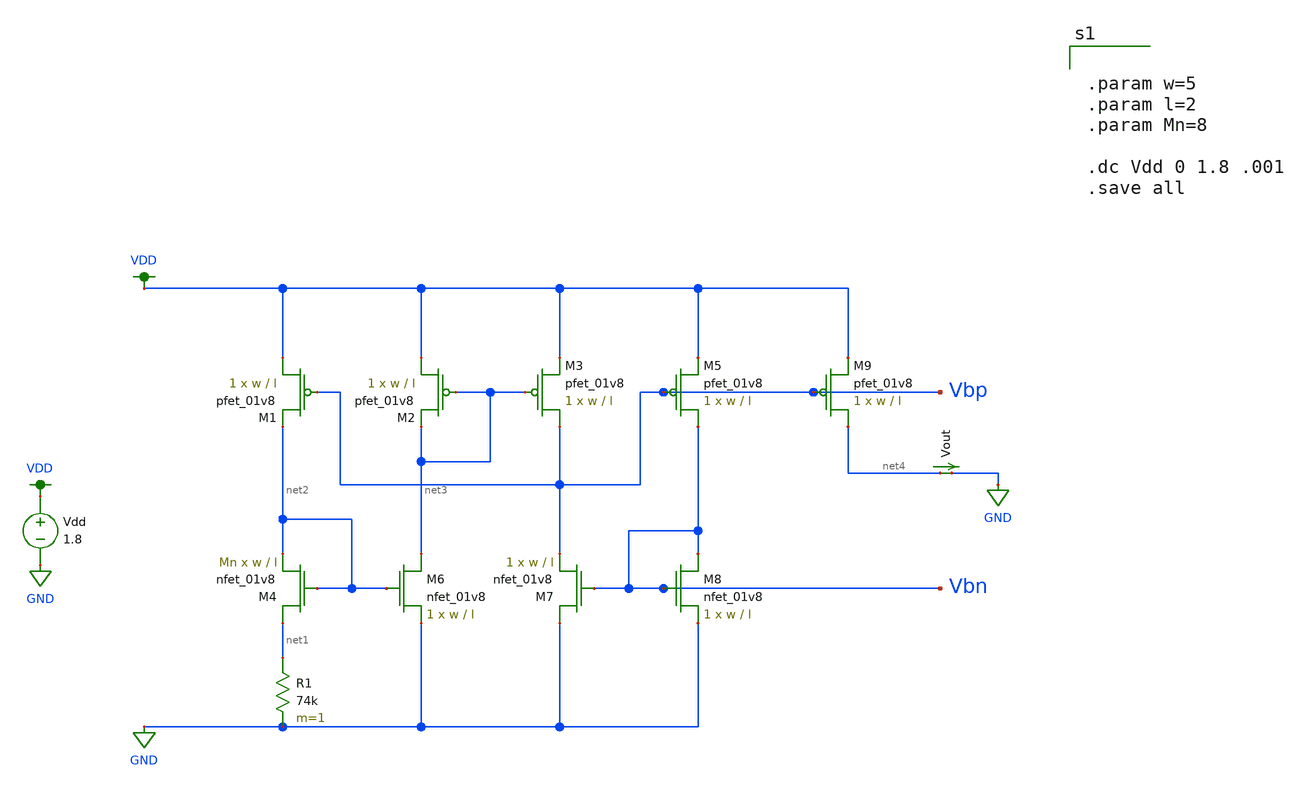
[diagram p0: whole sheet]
** sch_path: schematic/test/bias_current_resistive.sch
**.subckt bias_current_resistive
XM1 VDD Vbp net2 VDD sky130_fd_pr__pfet_01v8 L=l W=w nf=1 ad='int((nf+1)/2) * W/nf * 0.29' as='int((nf+2)/2) * W/nf * 0.29'
+ pd='2*int((nf+1)/2) * (W/nf + 0.29)' ps='2*int((nf+2)/2) * (W/nf + 0.29)' nrd='0.29 / W' nrs='0.29 / W'
+ sa=0 sb=0 sd=0 mult=1 m=1
XM2 VDD net3 net3 VDD sky130_fd_pr__pfet_01v8 L=l W=w nf=1 ad='int((nf+1)/2) * W/nf * 0.29' as='int((nf+2)/2) * W/nf * 0.29'
+ pd='2*int((nf+1)/2) * (W/nf + 0.29)' ps='2*int((nf+2)/2) * (W/nf + 0.29)' nrd='0.29 / W' nrs='0.29 / W'
+ sa=0 sb=0 sd=0 mult=1 m=1
XM3 Vbp net3 VDD VDD sky130_fd_pr__pfet_01v8 L=l W=w nf=1 ad='int((nf+1)/2) * W/nf * 0.29' as='int((nf+2)/2) * W/nf * 0.29'
+ pd='2*int((nf+1)/2) * (W/nf + 0.29)' ps='2*int((nf+2)/2) * (W/nf + 0.29)' nrd='0.29 / W' nrs='0.29 / W'
+ sa=0 sb=0 sd=0 mult=1 m=1
XM5 Vbn Vbp VDD VDD sky130_fd_pr__pfet_01v8 L=l W=w nf=1 ad='int((nf+1)/2) * W/nf * 0.29' as='int((nf+2)/2) * W/nf * 0.29'
+ pd='2*int((nf+1)/2) * (W/nf + 0.29)' ps='2*int((nf+2)/2) * (W/nf + 0.29)' nrd='0.29 / W' nrs='0.29 / W'
+ sa=0 sb=0 sd=0 mult=1 m=1
XM4 net1 net2 net2 GND sky130_fd_pr__nfet_01v8 L=l W=w nf=1 ad='int((nf+1)/2) * W/nf * 0.29' as='int((nf+2)/2) * W/nf * 0.29'
+ pd='2*int((nf+1)/2) * (W/nf + 0.29)' ps='2*int((nf+2)/2) * (W/nf + 0.29)' nrd='0.29 / W' nrs='0.29 / W'
+ sa=0 sb=0 sd=0 mult=Mn m=Mn
XM6 net3 net2 GND GND sky130_fd_pr__nfet_01v8 L=l W=w nf=1 ad='int((nf+1)/2) * W/nf * 0.29' as='int((nf+2)/2) * W/nf * 0.29'
+ pd='2*int((nf+1)/2) * (W/nf + 0.29)' ps='2*int((nf+2)/2) * (W/nf + 0.29)' nrd='0.29 / W' nrs='0.29 / W'
+ sa=0 sb=0 sd=0 mult=1 m=1
XM7 GND Vbn Vbp GND sky130_fd_pr__nfet_01v8 L=l W=w nf=1 ad='int((nf+1)/2) * W/nf * 0.29' as='int((nf+2)/2) * W/nf * 0.29'
+ pd='2*int((nf+1)/2) * (W/nf + 0.29)' ps='2*int((nf+2)/2) * (W/nf + 0.29)' nrd='0.29 / W' nrs='0.29 / W'
+ sa=0 sb=0 sd=0 mult=1 m=1
XM8 Vbn Vbn GND GND sky130_fd_pr__nfet_01v8 L=l W=w nf=1 ad='int((nf+1)/2) * W/nf * 0.29' as='int((nf+2)/2) * W/nf * 0.29'
+ pd='2*int((nf+1)/2) * (W/nf + 0.29)' ps='2*int((nf+2)/2) * (W/nf + 0.29)' nrd='0.29 / W' nrs='0.29 / W'
+ sa=0 sb=0 sd=0 mult=1 m=1
R1 net1 GND 74k m=1
XM9 net4 Vbp VDD VDD sky130_fd_pr__pfet_01v8 L=l W=w nf=1 ad='int((nf+1)/2) * W/nf * 0.29' as='int((nf+2)/2) * W/nf * 0.29'
+ pd='2*int((nf+1)/2) * (W/nf + 0.29)' ps='2*int((nf+2)/2) * (W/nf + 0.29)' nrd='0.29 / W' nrs='0.29 / W'
+ sa=0 sb=0 sd=0 mult=1 m=1
Vdd VDD GND 1.8
Vout net4 GND 0
.save i(vout)
**** begin user architecture code


.param w=5
.param l=2
.param Mn=8

.dc Vdd 0 1.8 .001
.save all




.option wnflag=1
.param MC_SWITCH=0.0
.lib ~/skywater/skywater-pdk/libraries/sky130_fd_pr_ngspice/latest/models/sky130.lib.spice tt

**** end user architecture code
**.ends
.GLOBAL VDD
.GLOBAL GND
.end
